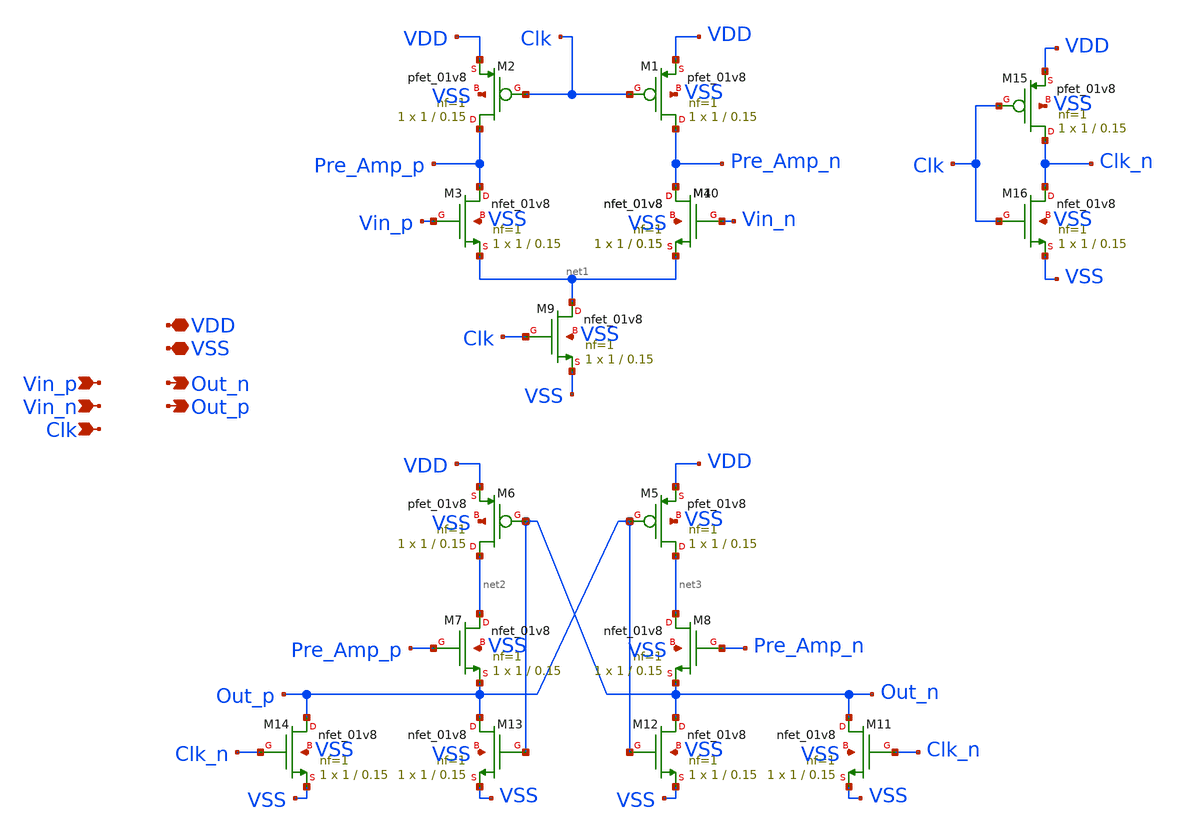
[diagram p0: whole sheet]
** sch_path: xschem/src/comparator/comparator.sch
**.subckt comparator VDD VSS Vin_p Out_n Vin_n Out_p Clk
*.iopin VDD
*.iopin VSS
*.ipin Vin_p
*.opin Out_n
*.ipin Vin_n
*.opin Out_p
*.ipin Clk
XM1 Pre_Amp_n Clk VDD VSS sky130_fd_pr__pfet_01v8 L=0.15 W=1 nf=1 ad='int((nf+1)/2) * W/nf * 0.29' as='int((nf+2)/2) * W/nf * 0.29'
+ pd='2*int((nf+1)/2) * (W/nf + 0.29)' ps='2*int((nf+2)/2) * (W/nf + 0.29)' nrd='0.29 / W' nrs='0.29 / W'
+ sa=0 sb=0 sd=0 mult=1 m=1
XM2 Pre_Amp_p Clk VDD VSS sky130_fd_pr__pfet_01v8 L=0.15 W=1 nf=1 ad='int((nf+1)/2) * W/nf * 0.29' as='int((nf+2)/2) * W/nf * 0.29'
+ pd='2*int((nf+1)/2) * (W/nf + 0.29)' ps='2*int((nf+2)/2) * (W/nf + 0.29)' nrd='0.29 / W' nrs='0.29 / W'
+ sa=0 sb=0 sd=0 mult=1 m=1
XM3 Pre_Amp_p Vin_p net1 VSS sky130_fd_pr__nfet_01v8 L=0.15 W=1 nf=1 ad='int((nf+1)/2) * W/nf * 0.29'
+ as='int((nf+2)/2) * W/nf * 0.29' pd='2*int((nf+1)/2) * (W/nf + 0.29)' ps='2*int((nf+2)/2) * (W/nf + 0.29)'
+ nrd='0.29 / W' nrs='0.29 / W' sa=0 sb=0 sd=0 mult=1 m=1
XM4 Pre_Amp_n Vin_n net1 VSS sky130_fd_pr__nfet_01v8 L=0.15 W=1 nf=1 ad='int((nf+1)/2) * W/nf * 0.29'
+ as='int((nf+2)/2) * W/nf * 0.29' pd='2*int((nf+1)/2) * (W/nf + 0.29)' ps='2*int((nf+2)/2) * (W/nf + 0.29)'
+ nrd='0.29 / W' nrs='0.29 / W' sa=0 sb=0 sd=0 mult=1 m=1
XM5 net3 Out_p VDD VSS sky130_fd_pr__pfet_01v8 L=0.15 W=1 nf=1 ad='int((nf+1)/2) * W/nf * 0.29' as='int((nf+2)/2) * W/nf * 0.29'
+ pd='2*int((nf+1)/2) * (W/nf + 0.29)' ps='2*int((nf+2)/2) * (W/nf + 0.29)' nrd='0.29 / W' nrs='0.29 / W'
+ sa=0 sb=0 sd=0 mult=1 m=1
XM6 net2 Out_n VDD VSS sky130_fd_pr__pfet_01v8 L=0.15 W=1 nf=1 ad='int((nf+1)/2) * W/nf * 0.29' as='int((nf+2)/2) * W/nf * 0.29'
+ pd='2*int((nf+1)/2) * (W/nf + 0.29)' ps='2*int((nf+2)/2) * (W/nf + 0.29)' nrd='0.29 / W' nrs='0.29 / W'
+ sa=0 sb=0 sd=0 mult=1 m=1
XM7 net2 Pre_Amp_p Out_p VSS sky130_fd_pr__nfet_01v8 L=0.15 W=1 nf=1 ad='int((nf+1)/2) * W/nf * 0.29'
+ as='int((nf+2)/2) * W/nf * 0.29' pd='2*int((nf+1)/2) * (W/nf + 0.29)' ps='2*int((nf+2)/2) * (W/nf + 0.29)'
+ nrd='0.29 / W' nrs='0.29 / W' sa=0 sb=0 sd=0 mult=1 m=1
XM8 net3 Pre_Amp_n Out_n VSS sky130_fd_pr__nfet_01v8 L=0.15 W=1 nf=1 ad='int((nf+1)/2) * W/nf * 0.29'
+ as='int((nf+2)/2) * W/nf * 0.29' pd='2*int((nf+1)/2) * (W/nf + 0.29)' ps='2*int((nf+2)/2) * (W/nf + 0.29)'
+ nrd='0.29 / W' nrs='0.29 / W' sa=0 sb=0 sd=0 mult=1 m=1
XM9 net1 Clk VSS VSS sky130_fd_pr__nfet_01v8 L=0.15 W=1 nf=1 ad='int((nf+1)/2) * W/nf * 0.29' as='int((nf+2)/2) * W/nf * 0.29'
+ pd='2*int((nf+1)/2) * (W/nf + 0.29)' ps='2*int((nf+2)/2) * (W/nf + 0.29)' nrd='0.29 / W' nrs='0.29 / W'
+ sa=0 sb=0 sd=0 mult=1 m=1
XM10 Pre_Amp_n Vin_n net1 VSS sky130_fd_pr__nfet_01v8 L=0.15 W=1 nf=1 ad='int((nf+1)/2) * W/nf * 0.29'
+ as='int((nf+2)/2) * W/nf * 0.29' pd='2*int((nf+1)/2) * (W/nf + 0.29)' ps='2*int((nf+2)/2) * (W/nf + 0.29)'
+ nrd='0.29 / W' nrs='0.29 / W' sa=0 sb=0 sd=0 mult=1 m=1
XM11 Out_n Clk_n VSS VSS sky130_fd_pr__nfet_01v8 L=0.15 W=1 nf=1 ad='int((nf+1)/2) * W/nf * 0.29' as='int((nf+2)/2) * W/nf * 0.29'
+ pd='2*int((nf+1)/2) * (W/nf + 0.29)' ps='2*int((nf+2)/2) * (W/nf + 0.29)' nrd='0.29 / W' nrs='0.29 / W'
+ sa=0 sb=0 sd=0 mult=1 m=1
XM12 Out_n Out_p VSS VSS sky130_fd_pr__nfet_01v8 L=0.15 W=1 nf=1 ad='int((nf+1)/2) * W/nf * 0.29' as='int((nf+2)/2) * W/nf * 0.29'
+ pd='2*int((nf+1)/2) * (W/nf + 0.29)' ps='2*int((nf+2)/2) * (W/nf + 0.29)' nrd='0.29 / W' nrs='0.29 / W'
+ sa=0 sb=0 sd=0 mult=1 m=1
XM13 Out_p Out_n VSS VSS sky130_fd_pr__nfet_01v8 L=0.15 W=1 nf=1 ad='int((nf+1)/2) * W/nf * 0.29' as='int((nf+2)/2) * W/nf * 0.29'
+ pd='2*int((nf+1)/2) * (W/nf + 0.29)' ps='2*int((nf+2)/2) * (W/nf + 0.29)' nrd='0.29 / W' nrs='0.29 / W'
+ sa=0 sb=0 sd=0 mult=1 m=1
XM14 Out_p Clk_n VSS VSS sky130_fd_pr__nfet_01v8 L=0.15 W=1 nf=1 ad='int((nf+1)/2) * W/nf * 0.29' as='int((nf+2)/2) * W/nf * 0.29'
+ pd='2*int((nf+1)/2) * (W/nf + 0.29)' ps='2*int((nf+2)/2) * (W/nf + 0.29)' nrd='0.29 / W' nrs='0.29 / W'
+ sa=0 sb=0 sd=0 mult=1 m=1
XM15 Clk_n Clk VDD VSS sky130_fd_pr__pfet_01v8 L=0.15 W=1 nf=1 ad='int((nf+1)/2) * W/nf * 0.29' as='int((nf+2)/2) * W/nf * 0.29'
+ pd='2*int((nf+1)/2) * (W/nf + 0.29)' ps='2*int((nf+2)/2) * (W/nf + 0.29)' nrd='0.29 / W' nrs='0.29 / W'
+ sa=0 sb=0 sd=0 mult=1 m=1
XM16 Clk_n Clk VSS VSS sky130_fd_pr__nfet_01v8 L=0.15 W=1 nf=1 ad='int((nf+1)/2) * W/nf * 0.29' as='int((nf+2)/2) * W/nf * 0.29'
+ pd='2*int((nf+1)/2) * (W/nf + 0.29)' ps='2*int((nf+2)/2) * (W/nf + 0.29)' nrd='0.29 / W' nrs='0.29 / W'
+ sa=0 sb=0 sd=0 mult=1 m=1
**.ends
.end
